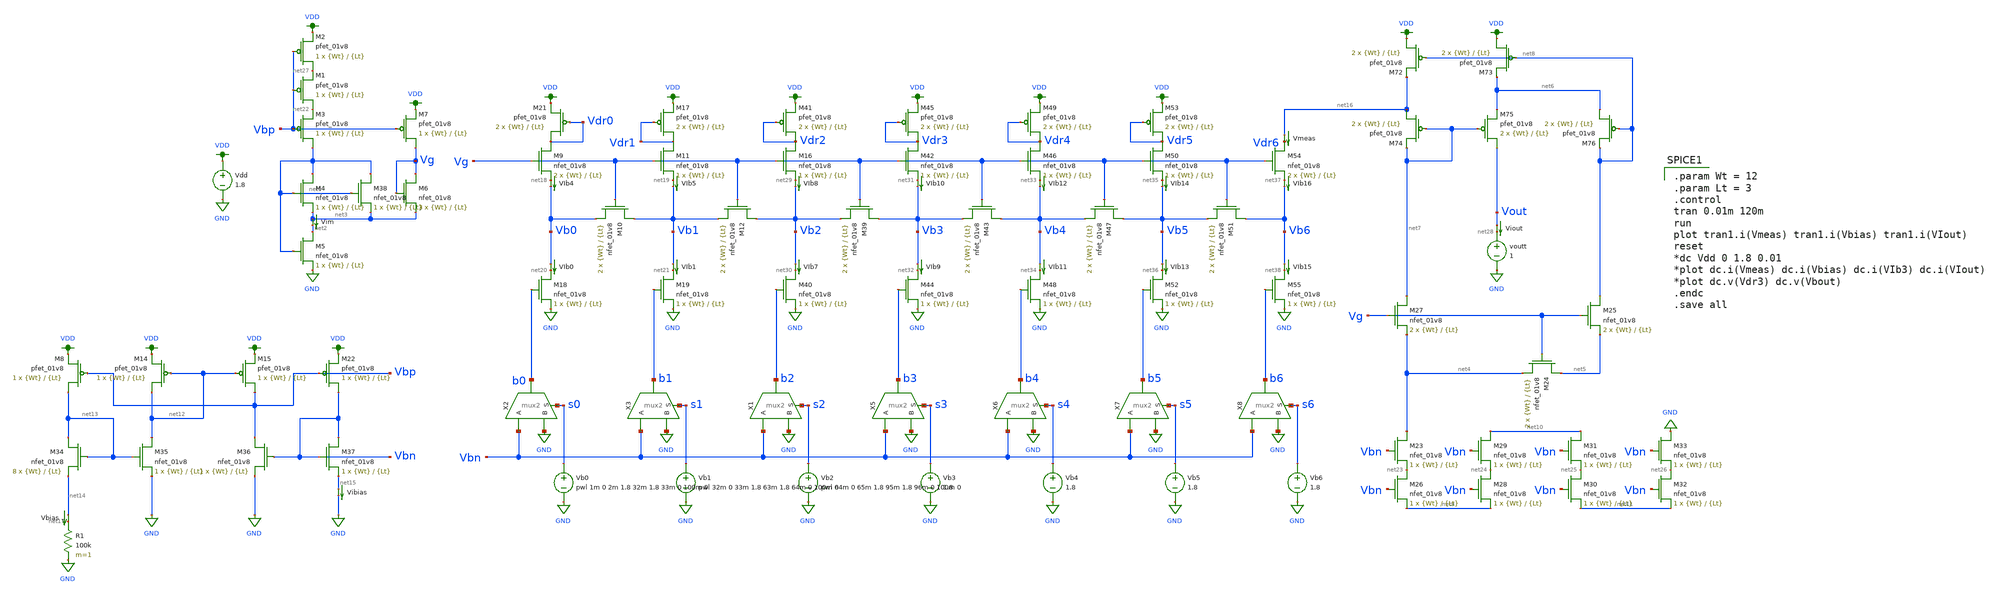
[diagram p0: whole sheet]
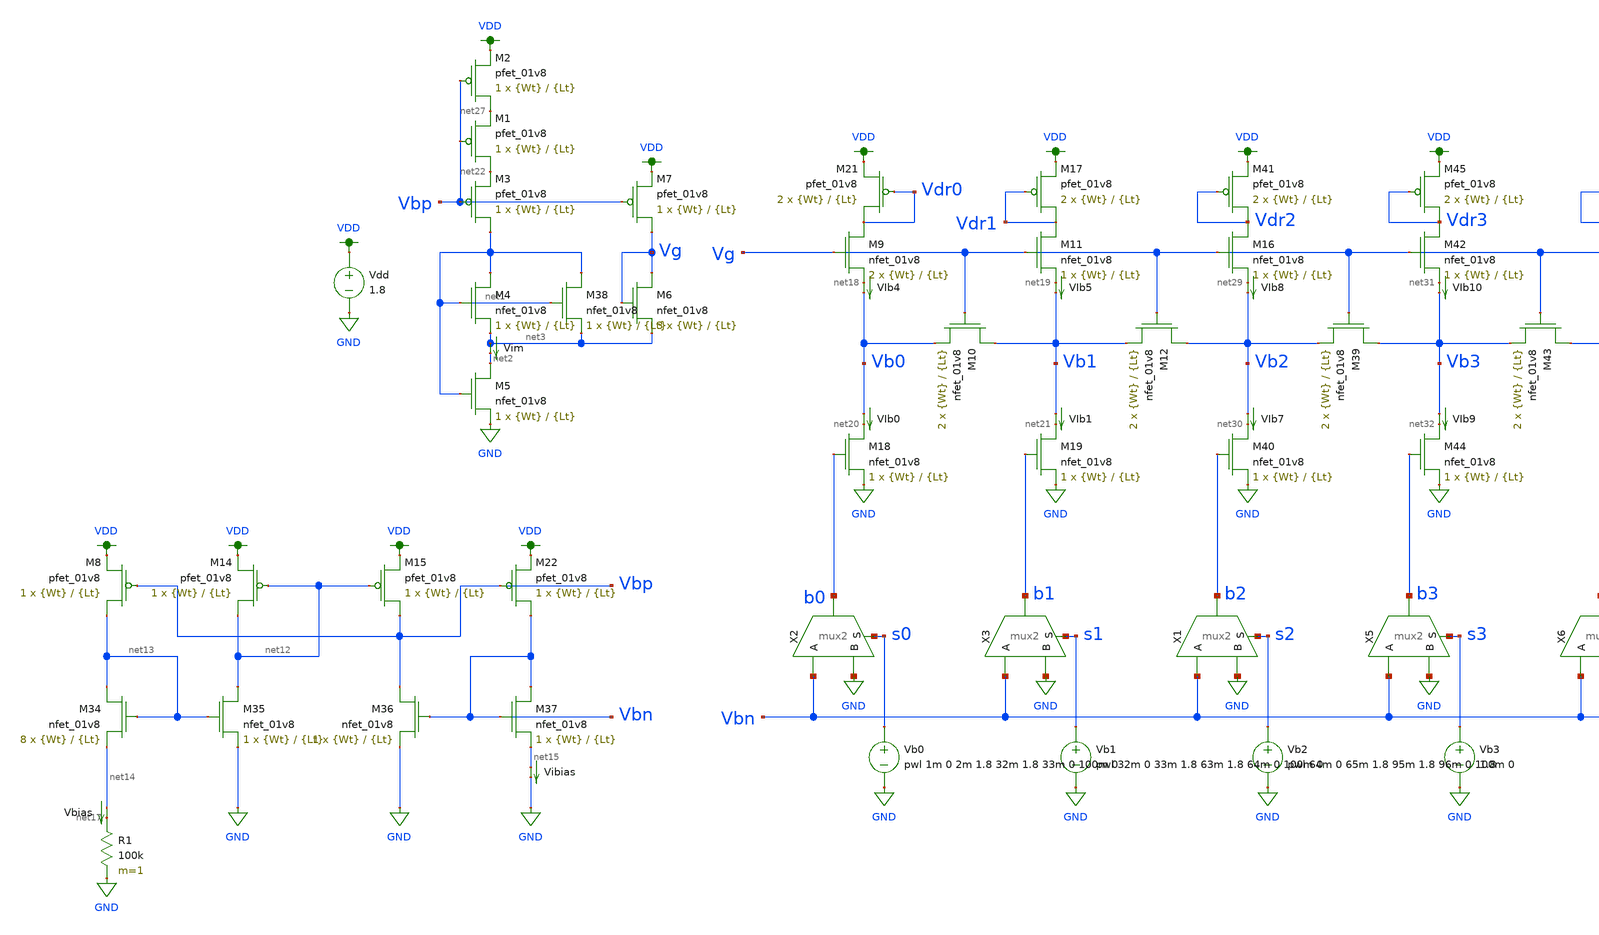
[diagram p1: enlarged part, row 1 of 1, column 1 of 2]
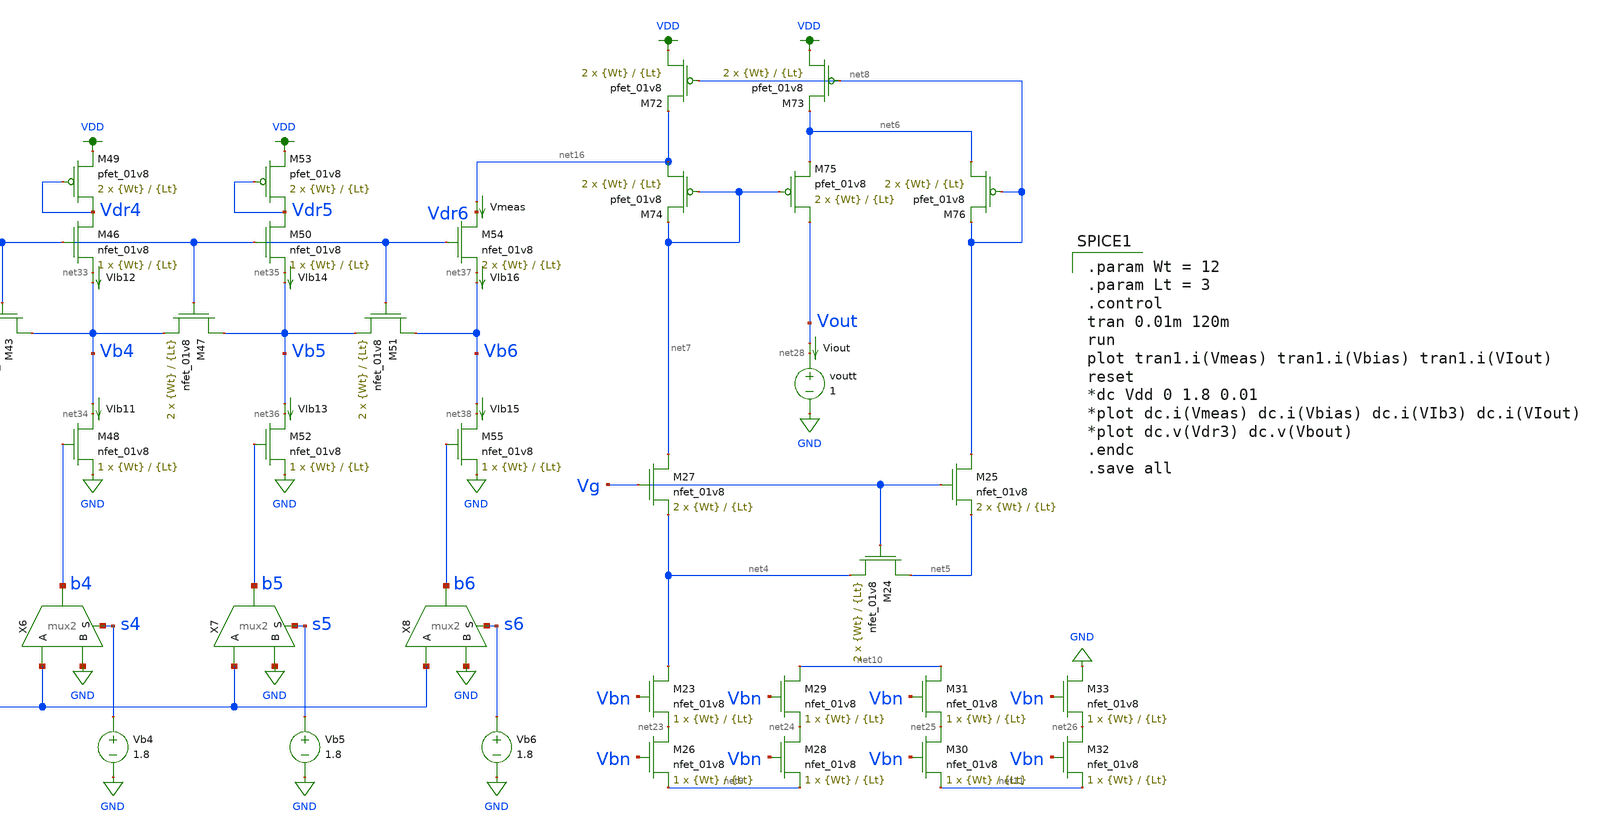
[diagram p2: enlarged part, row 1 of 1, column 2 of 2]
** sch_path: schematic/archive/dac7_test_SL_dynamic.sch
**.subckt dac7_test_SL_dynamic
X2 b0 Vbn GND s0 mux2
X3 b1 Vbn GND s1 mux2
R1 net17 GND 100k m=1
Vdd VDD GND 1.8
Vb0 s0 GND pwl 1m 0 2m 1.8 32m 1.8 33m 0 100m 0
Vb1 s1 GND pwl 32m 0 33m 1.8 63m 1.8 64m 0 100m 0
XM9 Vdr0 Vg net18 GND sky130_fd_pr__nfet_01v8 L={Lt} W={Wt} nf=1 ad='int((nf+1)/2) * W/nf * 0.29' as='int((nf+2)/2) * W/nf * 0.29'
+ pd='2*int((nf+1)/2) * (W/nf + 0.29)' ps='2*int((nf+2)/2) * (W/nf + 0.29)' nrd='0.29 / W' nrs='0.29 / W'
+ sa=0 sb=0 sd=0 mult=2 m=2
XM10 Vb1 Vg Vb0 GND sky130_fd_pr__nfet_01v8 L={Lt} W={Wt} nf=1 ad='int((nf+1)/2) * W/nf * 0.29' as='int((nf+2)/2) * W/nf * 0.29'
+ pd='2*int((nf+1)/2) * (W/nf + 0.29)' ps='2*int((nf+2)/2) * (W/nf + 0.29)' nrd='0.29 / W' nrs='0.29 / W'
+ sa=0 sb=0 sd=0 mult=2 m=2
XM11 Vdr1 Vg net19 GND sky130_fd_pr__nfet_01v8 L={Lt} W={Wt} nf=1 ad='int((nf+1)/2) * W/nf * 0.29' as='int((nf+2)/2) * W/nf * 0.29'
+ pd='2*int((nf+1)/2) * (W/nf + 0.29)' ps='2*int((nf+2)/2) * (W/nf + 0.29)' nrd='0.29 / W' nrs='0.29 / W'
+ sa=0 sb=0 sd=0 mult=1 m=1
XM12 Vb2 Vg Vb1 GND sky130_fd_pr__nfet_01v8 L={Lt} W={Wt} nf=1 ad='int((nf+1)/2) * W/nf * 0.29' as='int((nf+2)/2) * W/nf * 0.29'
+ pd='2*int((nf+1)/2) * (W/nf + 0.29)' ps='2*int((nf+2)/2) * (W/nf + 0.29)' nrd='0.29 / W' nrs='0.29 / W'
+ sa=0 sb=0 sd=0 mult=2 m=2
XM18 net20 b0 GND GND sky130_fd_pr__nfet_01v8 L={Lt} W={Wt} nf=1 ad='int((nf+1)/2) * W/nf * 0.29' as='int((nf+2)/2) * W/nf * 0.29'
+ pd='2*int((nf+1)/2) * (W/nf + 0.29)' ps='2*int((nf+2)/2) * (W/nf + 0.29)' nrd='0.29 / W' nrs='0.29 / W'
+ sa=0 sb=0 sd=0 mult=1 m=1
XM19 net21 b1 GND GND sky130_fd_pr__nfet_01v8 L={Lt} W={Wt} nf=1 ad='int((nf+1)/2) * W/nf * 0.29' as='int((nf+2)/2) * W/nf * 0.29'
+ pd='2*int((nf+1)/2) * (W/nf + 0.29)' ps='2*int((nf+2)/2) * (W/nf + 0.29)' nrd='0.29 / W' nrs='0.29 / W'
+ sa=0 sb=0 sd=0 mult=1 m=1
Vbias net14 net17 0
.save i(vbias)
VIb0 Vb0 net20 0
.save i(vib0)
VIb1 Vb1 net21 0
.save i(vib1)
XM3 net1 Vbp net22 VDD sky130_fd_pr__pfet_01v8 L={Lt} W={Wt} nf=1 ad='int((nf+1)/2) * W/nf * 0.29' as='int((nf+2)/2) * W/nf * 0.29'
+ pd='2*int((nf+1)/2) * (W/nf + 0.29)' ps='2*int((nf+2)/2) * (W/nf + 0.29)' nrd='0.29 / W' nrs='0.29 / W'
+ sa=0 sb=0 sd=0 mult=1 m=1
XM4 net1 net1 net3 GND sky130_fd_pr__nfet_01v8 L={Lt} W={Wt} nf=1 ad='int((nf+1)/2) * W/nf * 0.29' as='int((nf+2)/2) * W/nf * 0.29'
+ pd='2*int((nf+1)/2) * (W/nf + 0.29)' ps='2*int((nf+2)/2) * (W/nf + 0.29)' nrd='0.29 / W' nrs='0.29 / W'
+ sa=0 sb=0 sd=0 mult=1 m=1
XM5 net2 net1 GND GND sky130_fd_pr__nfet_01v8 L={Lt} W={Wt} nf=1 ad='int((nf+1)/2) * W/nf * 0.29' as='int((nf+2)/2) * W/nf * 0.29'
+ pd='2*int((nf+1)/2) * (W/nf + 0.29)' ps='2*int((nf+2)/2) * (W/nf + 0.29)' nrd='0.29 / W' nrs='0.29 / W'
+ sa=0 sb=0 sd=0 mult=1 m=1
Vim net3 net2 0
.save i(vim)
XM6 Vg Vg net3 GND sky130_fd_pr__nfet_01v8 L={Lt} W={Wt} nf=1 ad='int((nf+1)/2) * W/nf * 0.29' as='int((nf+2)/2) * W/nf * 0.29'
+ pd='2*int((nf+1)/2) * (W/nf + 0.29)' ps='2*int((nf+2)/2) * (W/nf + 0.29)' nrd='0.29 / W' nrs='0.29 / W'
+ sa=0 sb=0 sd=0 mult=3 m=3
XM7 Vg Vbp VDD VDD sky130_fd_pr__pfet_01v8 L={Lt} W={Wt} nf=1 ad='int((nf+1)/2) * W/nf * 0.29' as='int((nf+2)/2) * W/nf * 0.29'
+ pd='2*int((nf+1)/2) * (W/nf + 0.29)' ps='2*int((nf+2)/2) * (W/nf + 0.29)' nrd='0.29 / W' nrs='0.29 / W'
+ sa=0 sb=0 sd=0 mult=1 m=1
XM17 Vdr1 Vdr1 VDD VDD sky130_fd_pr__pfet_01v8 L={Lt} W={Wt} nf=1 ad='int((nf+1)/2) * W/nf * 0.29' as='int((nf+2)/2) * W/nf * 0.29'
+ pd='2*int((nf+1)/2) * (W/nf + 0.29)' ps='2*int((nf+2)/2) * (W/nf + 0.29)' nrd='0.29 / W' nrs='0.29 / W'
+ sa=0 sb=0 sd=0 mult=2 m=2
XM21 Vdr0 Vdr0 VDD VDD sky130_fd_pr__pfet_01v8 L={Lt} W={Wt} nf=1 ad='int((nf+1)/2) * W/nf * 0.29' as='int((nf+2)/2) * W/nf * 0.29'
+ pd='2*int((nf+1)/2) * (W/nf + 0.29)' ps='2*int((nf+2)/2) * (W/nf + 0.29)' nrd='0.29 / W' nrs='0.29 / W'
+ sa=0 sb=0 sd=0 mult=2 m=2
VIb4 net18 Vb0 0
.save i(vib4)
VIb5 net19 Vb1 0
.save i(vib5)
XM24 net5 Vg net4 GND sky130_fd_pr__nfet_01v8 L={Lt} W={Wt} nf=1 ad='int((nf+1)/2) * W/nf * 0.29' as='int((nf+2)/2) * W/nf * 0.29'
+ pd='2*int((nf+1)/2) * (W/nf + 0.29)' ps='2*int((nf+2)/2) * (W/nf + 0.29)' nrd='0.29 / W' nrs='0.29 / W'
+ sa=0 sb=0 sd=0 mult=2 m=2
XM25 net8 Vg net5 GND sky130_fd_pr__nfet_01v8 L={Lt} W={Wt} nf=1 ad='int((nf+1)/2) * W/nf * 0.29' as='int((nf+2)/2) * W/nf * 0.29'
+ pd='2*int((nf+1)/2) * (W/nf + 0.29)' ps='2*int((nf+2)/2) * (W/nf + 0.29)' nrd='0.29 / W' nrs='0.29 / W'
+ sa=0 sb=0 sd=0 mult=2 m=2
XM26 net23 Vbn net9 GND sky130_fd_pr__nfet_01v8 L={Lt} W={Wt} nf=1 ad='int((nf+1)/2) * W/nf * 0.29' as='int((nf+2)/2) * W/nf * 0.29'
+ pd='2*int((nf+1)/2) * (W/nf + 0.29)' ps='2*int((nf+2)/2) * (W/nf + 0.29)' nrd='0.29 / W' nrs='0.29 / W'
+ sa=0 sb=0 sd=0 mult=1 m=1
XM27 net7 Vg net4 GND sky130_fd_pr__nfet_01v8 L={Lt} W={Wt} nf=1 ad='int((nf+1)/2) * W/nf * 0.29' as='int((nf+2)/2) * W/nf * 0.29'
+ pd='2*int((nf+1)/2) * (W/nf + 0.29)' ps='2*int((nf+2)/2) * (W/nf + 0.29)' nrd='0.29 / W' nrs='0.29 / W'
+ sa=0 sb=0 sd=0 mult=2 m=2
XM72 VDD net8 net16 VDD sky130_fd_pr__pfet_01v8 L={Lt} W={Wt} nf=1 ad='int((nf+1)/2) * W/nf * 0.29' as='int((nf+2)/2) * W/nf * 0.29'
+ pd='2*int((nf+1)/2) * (W/nf + 0.29)' ps='2*int((nf+2)/2) * (W/nf + 0.29)' nrd='0.29 / W' nrs='0.29 / W'
+ sa=0 sb=0 sd=0 mult=2 m=2
XM73 VDD net8 net6 VDD sky130_fd_pr__pfet_01v8 L={Lt} W={Wt} nf=1 ad='int((nf+1)/2) * W/nf * 0.29' as='int((nf+2)/2) * W/nf * 0.29'
+ pd='2*int((nf+1)/2) * (W/nf + 0.29)' ps='2*int((nf+2)/2) * (W/nf + 0.29)' nrd='0.29 / W' nrs='0.29 / W'
+ sa=0 sb=0 sd=0 mult=2 m=2
XM74 net16 net7 net7 VDD sky130_fd_pr__pfet_01v8 L={Lt} W={Wt} nf=1 ad='int((nf+1)/2) * W/nf * 0.29'
+ as='int((nf+2)/2) * W/nf * 0.29' pd='2*int((nf+1)/2) * (W/nf + 0.29)' ps='2*int((nf+2)/2) * (W/nf + 0.29)'
+ nrd='0.29 / W' nrs='0.29 / W' sa=0 sb=0 sd=0 mult=2 m=2
XM75 Vout net7 net6 VDD sky130_fd_pr__pfet_01v8 L={Lt} W={Wt} nf=1 ad='int((nf+1)/2) * W/nf * 0.29' as='int((nf+2)/2) * W/nf * 0.29'
+ pd='2*int((nf+1)/2) * (W/nf + 0.29)' ps='2*int((nf+2)/2) * (W/nf + 0.29)' nrd='0.29 / W' nrs='0.29 / W'
+ sa=0 sb=0 sd=0 mult=2 m=2
XM76 net6 net8 net8 VDD sky130_fd_pr__pfet_01v8 L={Lt} W={Wt} nf=1 ad='int((nf+1)/2) * W/nf * 0.29' as='int((nf+2)/2) * W/nf * 0.29'
+ pd='2*int((nf+1)/2) * (W/nf + 0.29)' ps='2*int((nf+2)/2) * (W/nf + 0.29)' nrd='0.29 / W' nrs='0.29 / W'
+ sa=0 sb=0 sd=0 mult=2 m=2
XM23 net4 Vbn net23 GND sky130_fd_pr__nfet_01v8 L={Lt} W={Wt} nf=1 ad='int((nf+1)/2) * W/nf * 0.29' as='int((nf+2)/2) * W/nf * 0.29'
+ pd='2*int((nf+1)/2) * (W/nf + 0.29)' ps='2*int((nf+2)/2) * (W/nf + 0.29)' nrd='0.29 / W' nrs='0.29 / W'
+ sa=0 sb=0 sd=0 mult=1 m=1
XM28 net24 Vbn net9 GND sky130_fd_pr__nfet_01v8 L={Lt} W={Wt} nf=1 ad='int((nf+1)/2) * W/nf * 0.29' as='int((nf+2)/2) * W/nf * 0.29'
+ pd='2*int((nf+1)/2) * (W/nf + 0.29)' ps='2*int((nf+2)/2) * (W/nf + 0.29)' nrd='0.29 / W' nrs='0.29 / W'
+ sa=0 sb=0 sd=0 mult=1 m=1
XM29 net10 Vbn net24 GND sky130_fd_pr__nfet_01v8 L={Lt} W={Wt} nf=1 ad='int((nf+1)/2) * W/nf * 0.29'
+ as='int((nf+2)/2) * W/nf * 0.29' pd='2*int((nf+1)/2) * (W/nf + 0.29)' ps='2*int((nf+2)/2) * (W/nf + 0.29)'
+ nrd='0.29 / W' nrs='0.29 / W' sa=0 sb=0 sd=0 mult=1 m=1
XM30 net25 Vbn net11 GND sky130_fd_pr__nfet_01v8 L={Lt} W={Wt} nf=1 ad='int((nf+1)/2) * W/nf * 0.29'
+ as='int((nf+2)/2) * W/nf * 0.29' pd='2*int((nf+1)/2) * (W/nf + 0.29)' ps='2*int((nf+2)/2) * (W/nf + 0.29)'
+ nrd='0.29 / W' nrs='0.29 / W' sa=0 sb=0 sd=0 mult=1 m=1
XM31 net10 Vbn net25 GND sky130_fd_pr__nfet_01v8 L={Lt} W={Wt} nf=1 ad='int((nf+1)/2) * W/nf * 0.29'
+ as='int((nf+2)/2) * W/nf * 0.29' pd='2*int((nf+1)/2) * (W/nf + 0.29)' ps='2*int((nf+2)/2) * (W/nf + 0.29)'
+ nrd='0.29 / W' nrs='0.29 / W' sa=0 sb=0 sd=0 mult=1 m=1
XM32 net26 Vbn net11 GND sky130_fd_pr__nfet_01v8 L={Lt} W={Wt} nf=1 ad='int((nf+1)/2) * W/nf * 0.29'
+ as='int((nf+2)/2) * W/nf * 0.29' pd='2*int((nf+1)/2) * (W/nf + 0.29)' ps='2*int((nf+2)/2) * (W/nf + 0.29)'
+ nrd='0.29 / W' nrs='0.29 / W' sa=0 sb=0 sd=0 mult=1 m=1
XM33 GND Vbn net26 GND sky130_fd_pr__nfet_01v8 L={Lt} W={Wt} nf=1 ad='int((nf+1)/2) * W/nf * 0.29' as='int((nf+2)/2) * W/nf * 0.29'
+ pd='2*int((nf+1)/2) * (W/nf + 0.29)' ps='2*int((nf+2)/2) * (W/nf + 0.29)' nrd='0.29 / W' nrs='0.29 / W'
+ sa=0 sb=0 sd=0 mult=1 m=1
XM8 net13 Vbp VDD VDD sky130_fd_pr__pfet_01v8 L={Lt} W={Wt} nf=1 ad='int((nf+1)/2) * W/nf * 0.29' as='int((nf+2)/2) * W/nf * 0.29'
+ pd='2*int((nf+1)/2) * (W/nf + 0.29)' ps='2*int((nf+2)/2) * (W/nf + 0.29)' nrd='0.29 / W' nrs='0.29 / W'
+ sa=0 sb=0 sd=0 mult=1 m=1
XM14 net12 net12 VDD VDD sky130_fd_pr__pfet_01v8 L={Lt} W={Wt} nf=1 ad='int((nf+1)/2) * W/nf * 0.29'
+ as='int((nf+2)/2) * W/nf * 0.29' pd='2*int((nf+1)/2) * (W/nf + 0.29)' ps='2*int((nf+2)/2) * (W/nf + 0.29)'
+ nrd='0.29 / W' nrs='0.29 / W' sa=0 sb=0 sd=0 mult=1 m=1
XM15 Vbp net12 VDD VDD sky130_fd_pr__pfet_01v8 L={Lt} W={Wt} nf=1 ad='int((nf+1)/2) * W/nf * 0.29' as='int((nf+2)/2) * W/nf * 0.29'
+ pd='2*int((nf+1)/2) * (W/nf + 0.29)' ps='2*int((nf+2)/2) * (W/nf + 0.29)' nrd='0.29 / W' nrs='0.29 / W'
+ sa=0 sb=0 sd=0 mult=1 m=1
XM22 Vbn Vbp VDD VDD sky130_fd_pr__pfet_01v8 L={Lt} W={Wt} nf=1 ad='int((nf+1)/2) * W/nf * 0.29' as='int((nf+2)/2) * W/nf * 0.29'
+ pd='2*int((nf+1)/2) * (W/nf + 0.29)' ps='2*int((nf+2)/2) * (W/nf + 0.29)' nrd='0.29 / W' nrs='0.29 / W'
+ sa=0 sb=0 sd=0 mult=1 m=1
XM34 net13 net13 net14 GND sky130_fd_pr__nfet_01v8 L={Lt} W={Wt} nf=1 ad='int((nf+1)/2) * W/nf * 0.29'
+ as='int((nf+2)/2) * W/nf * 0.29' pd='2*int((nf+1)/2) * (W/nf + 0.29)' ps='2*int((nf+2)/2) * (W/nf + 0.29)'
+ nrd='0.29 / W' nrs='0.29 / W' sa=0 sb=0 sd=0 mult=8 m=8
XM35 net12 net13 GND GND sky130_fd_pr__nfet_01v8 L={Lt} W={Wt} nf=1 ad='int((nf+1)/2) * W/nf * 0.29'
+ as='int((nf+2)/2) * W/nf * 0.29' pd='2*int((nf+1)/2) * (W/nf + 0.29)' ps='2*int((nf+2)/2) * (W/nf + 0.29)'
+ nrd='0.29 / W' nrs='0.29 / W' sa=0 sb=0 sd=0 mult=1 m=1
XM36 Vbp Vbn GND GND sky130_fd_pr__nfet_01v8 L={Lt} W={Wt} nf=1 ad='int((nf+1)/2) * W/nf * 0.29' as='int((nf+2)/2) * W/nf * 0.29'
+ pd='2*int((nf+1)/2) * (W/nf + 0.29)' ps='2*int((nf+2)/2) * (W/nf + 0.29)' nrd='0.29 / W' nrs='0.29 / W'
+ sa=0 sb=0 sd=0 mult=1 m=1
XM37 Vbn Vbn net15 GND sky130_fd_pr__nfet_01v8 L={Lt} W={Wt} nf=1 ad='int((nf+1)/2) * W/nf * 0.29' as='int((nf+2)/2) * W/nf * 0.29'
+ pd='2*int((nf+1)/2) * (W/nf + 0.29)' ps='2*int((nf+2)/2) * (W/nf + 0.29)' nrd='0.29 / W' nrs='0.29 / W'
+ sa=0 sb=0 sd=0 mult=1 m=1
Vibias net15 GND 0
.save i(vibias)
XM1 net22 Vbp net27 VDD sky130_fd_pr__pfet_01v8 L={Lt} W={Wt} nf=1 ad='int((nf+1)/2) * W/nf * 0.29' as='int((nf+2)/2) * W/nf * 0.29'
+ pd='2*int((nf+1)/2) * (W/nf + 0.29)' ps='2*int((nf+2)/2) * (W/nf + 0.29)' nrd='0.29 / W' nrs='0.29 / W'
+ sa=0 sb=0 sd=0 mult=1 m=1
XM2 net27 Vbp VDD VDD sky130_fd_pr__pfet_01v8 L={Lt} W={Wt} nf=1 ad='int((nf+1)/2) * W/nf * 0.29' as='int((nf+2)/2) * W/nf * 0.29'
+ pd='2*int((nf+1)/2) * (W/nf + 0.29)' ps='2*int((nf+2)/2) * (W/nf + 0.29)' nrd='0.29 / W' nrs='0.29 / W'
+ sa=0 sb=0 sd=0 mult=1 m=1
XM38 net1 net1 net3 GND sky130_fd_pr__nfet_01v8 L={Lt} W={Wt} nf=1 ad='int((nf+1)/2) * W/nf * 0.29' as='int((nf+2)/2) * W/nf * 0.29'
+ pd='2*int((nf+1)/2) * (W/nf + 0.29)' ps='2*int((nf+2)/2) * (W/nf + 0.29)' nrd='0.29 / W' nrs='0.29 / W'
+ sa=0 sb=0 sd=0 mult=1 m=1
voutt net28 GND 1
X1 b2 Vbn GND s2 mux2
Vb3 s3 GND 1.8
XM16 Vdr2 Vg net29 GND sky130_fd_pr__nfet_01v8 L={Lt} W={Wt} nf=1 ad='int((nf+1)/2) * W/nf * 0.29' as='int((nf+2)/2) * W/nf * 0.29'
+ pd='2*int((nf+1)/2) * (W/nf + 0.29)' ps='2*int((nf+2)/2) * (W/nf + 0.29)' nrd='0.29 / W' nrs='0.29 / W'
+ sa=0 sb=0 sd=0 mult=1 m=1
XM39 Vb3 Vg Vb2 GND sky130_fd_pr__nfet_01v8 L={Lt} W={Wt} nf=1 ad='int((nf+1)/2) * W/nf * 0.29' as='int((nf+2)/2) * W/nf * 0.29'
+ pd='2*int((nf+1)/2) * (W/nf + 0.29)' ps='2*int((nf+2)/2) * (W/nf + 0.29)' nrd='0.29 / W' nrs='0.29 / W'
+ sa=0 sb=0 sd=0 mult=2 m=2
XM40 net30 b2 GND GND sky130_fd_pr__nfet_01v8 L={Lt} W={Wt} nf=1 ad='int((nf+1)/2) * W/nf * 0.29' as='int((nf+2)/2) * W/nf * 0.29'
+ pd='2*int((nf+1)/2) * (W/nf + 0.29)' ps='2*int((nf+2)/2) * (W/nf + 0.29)' nrd='0.29 / W' nrs='0.29 / W'
+ sa=0 sb=0 sd=0 mult=1 m=1
VIb7 Vb2 net30 0
.save i(vib7)
XM41 Vdr2 Vdr2 VDD VDD sky130_fd_pr__pfet_01v8 L={Lt} W={Wt} nf=1 ad='int((nf+1)/2) * W/nf * 0.29' as='int((nf+2)/2) * W/nf * 0.29'
+ pd='2*int((nf+1)/2) * (W/nf + 0.29)' ps='2*int((nf+2)/2) * (W/nf + 0.29)' nrd='0.29 / W' nrs='0.29 / W'
+ sa=0 sb=0 sd=0 mult=2 m=2
VIb8 net29 Vb2 0
.save i(vib8)
X5 b3 Vbn GND s3 mux2
Vb4 s4 GND 1.8
XM42 Vdr3 Vg net31 GND sky130_fd_pr__nfet_01v8 L={Lt} W={Wt} nf=1 ad='int((nf+1)/2) * W/nf * 0.29' as='int((nf+2)/2) * W/nf * 0.29'
+ pd='2*int((nf+1)/2) * (W/nf + 0.29)' ps='2*int((nf+2)/2) * (W/nf + 0.29)' nrd='0.29 / W' nrs='0.29 / W'
+ sa=0 sb=0 sd=0 mult=1 m=1
XM43 Vb4 Vg Vb3 GND sky130_fd_pr__nfet_01v8 L={Lt} W={Wt} nf=1 ad='int((nf+1)/2) * W/nf * 0.29' as='int((nf+2)/2) * W/nf * 0.29'
+ pd='2*int((nf+1)/2) * (W/nf + 0.29)' ps='2*int((nf+2)/2) * (W/nf + 0.29)' nrd='0.29 / W' nrs='0.29 / W'
+ sa=0 sb=0 sd=0 mult=2 m=2
XM44 net32 b3 GND GND sky130_fd_pr__nfet_01v8 L={Lt} W={Wt} nf=1 ad='int((nf+1)/2) * W/nf * 0.29' as='int((nf+2)/2) * W/nf * 0.29'
+ pd='2*int((nf+1)/2) * (W/nf + 0.29)' ps='2*int((nf+2)/2) * (W/nf + 0.29)' nrd='0.29 / W' nrs='0.29 / W'
+ sa=0 sb=0 sd=0 mult=1 m=1
VIb9 Vb3 net32 0
.save i(vib9)
XM45 Vdr3 Vdr3 VDD VDD sky130_fd_pr__pfet_01v8 L={Lt} W={Wt} nf=1 ad='int((nf+1)/2) * W/nf * 0.29' as='int((nf+2)/2) * W/nf * 0.29'
+ pd='2*int((nf+1)/2) * (W/nf + 0.29)' ps='2*int((nf+2)/2) * (W/nf + 0.29)' nrd='0.29 / W' nrs='0.29 / W'
+ sa=0 sb=0 sd=0 mult=2 m=2
VIb10 net31 Vb3 0
.save i(vib10)
X6 b4 Vbn GND s4 mux2
Vb5 s5 GND 1.8
XM46 Vdr4 Vg net33 GND sky130_fd_pr__nfet_01v8 L={Lt} W={Wt} nf=1 ad='int((nf+1)/2) * W/nf * 0.29' as='int((nf+2)/2) * W/nf * 0.29'
+ pd='2*int((nf+1)/2) * (W/nf + 0.29)' ps='2*int((nf+2)/2) * (W/nf + 0.29)' nrd='0.29 / W' nrs='0.29 / W'
+ sa=0 sb=0 sd=0 mult=1 m=1
XM47 Vb5 Vg Vb4 GND sky130_fd_pr__nfet_01v8 L={Lt} W={Wt} nf=1 ad='int((nf+1)/2) * W/nf * 0.29' as='int((nf+2)/2) * W/nf * 0.29'
+ pd='2*int((nf+1)/2) * (W/nf + 0.29)' ps='2*int((nf+2)/2) * (W/nf + 0.29)' nrd='0.29 / W' nrs='0.29 / W'
+ sa=0 sb=0 sd=0 mult=2 m=2
XM48 net34 b4 GND GND sky130_fd_pr__nfet_01v8 L={Lt} W={Wt} nf=1 ad='int((nf+1)/2) * W/nf * 0.29' as='int((nf+2)/2) * W/nf * 0.29'
+ pd='2*int((nf+1)/2) * (W/nf + 0.29)' ps='2*int((nf+2)/2) * (W/nf + 0.29)' nrd='0.29 / W' nrs='0.29 / W'
+ sa=0 sb=0 sd=0 mult=1 m=1
VIb11 Vb4 net34 0
.save i(vib11)
XM49 Vdr4 Vdr4 VDD VDD sky130_fd_pr__pfet_01v8 L={Lt} W={Wt} nf=1 ad='int((nf+1)/2) * W/nf * 0.29' as='int((nf+2)/2) * W/nf * 0.29'
+ pd='2*int((nf+1)/2) * (W/nf + 0.29)' ps='2*int((nf+2)/2) * (W/nf + 0.29)' nrd='0.29 / W' nrs='0.29 / W'
+ sa=0 sb=0 sd=0 mult=2 m=2
VIb12 net33 Vb4 0
.save i(vib12)
X7 b5 Vbn GND s5 mux2
Vb6 s6 GND 1.8
XM50 Vdr5 Vg net35 GND sky130_fd_pr__nfet_01v8 L={Lt} W={Wt} nf=1 ad='int((nf+1)/2) * W/nf * 0.29' as='int((nf+2)/2) * W/nf * 0.29'
+ pd='2*int((nf+1)/2) * (W/nf + 0.29)' ps='2*int((nf+2)/2) * (W/nf + 0.29)' nrd='0.29 / W' nrs='0.29 / W'
+ sa=0 sb=0 sd=0 mult=1 m=1
XM51 Vb6 Vg Vb5 GND sky130_fd_pr__nfet_01v8 L={Lt} W={Wt} nf=1 ad='int((nf+1)/2) * W/nf * 0.29' as='int((nf+2)/2) * W/nf * 0.29'
+ pd='2*int((nf+1)/2) * (W/nf + 0.29)' ps='2*int((nf+2)/2) * (W/nf + 0.29)' nrd='0.29 / W' nrs='0.29 / W'
+ sa=0 sb=0 sd=0 mult=2 m=2
XM52 net36 b5 GND GND sky130_fd_pr__nfet_01v8 L={Lt} W={Wt} nf=1 ad='int((nf+1)/2) * W/nf * 0.29' as='int((nf+2)/2) * W/nf * 0.29'
+ pd='2*int((nf+1)/2) * (W/nf + 0.29)' ps='2*int((nf+2)/2) * (W/nf + 0.29)' nrd='0.29 / W' nrs='0.29 / W'
+ sa=0 sb=0 sd=0 mult=1 m=1
VIb13 Vb5 net36 0
.save i(vib13)
XM53 Vdr5 Vdr5 VDD VDD sky130_fd_pr__pfet_01v8 L={Lt} W={Wt} nf=1 ad='int((nf+1)/2) * W/nf * 0.29' as='int((nf+2)/2) * W/nf * 0.29'
+ pd='2*int((nf+1)/2) * (W/nf + 0.29)' ps='2*int((nf+2)/2) * (W/nf + 0.29)' nrd='0.29 / W' nrs='0.29 / W'
+ sa=0 sb=0 sd=0 mult=2 m=2
VIb14 net35 Vb5 0
.save i(vib14)
X8 b6 Vbn GND s6 mux2
XM54 Vdr6 Vg net37 GND sky130_fd_pr__nfet_01v8 L={Lt} W={Wt} nf=1 ad='int((nf+1)/2) * W/nf * 0.29' as='int((nf+2)/2) * W/nf * 0.29'
+ pd='2*int((nf+1)/2) * (W/nf + 0.29)' ps='2*int((nf+2)/2) * (W/nf + 0.29)' nrd='0.29 / W' nrs='0.29 / W'
+ sa=0 sb=0 sd=0 mult=2 m=2
XM55 net38 b6 GND GND sky130_fd_pr__nfet_01v8 L={Lt} W={Wt} nf=1 ad='int((nf+1)/2) * W/nf * 0.29' as='int((nf+2)/2) * W/nf * 0.29'
+ pd='2*int((nf+1)/2) * (W/nf + 0.29)' ps='2*int((nf+2)/2) * (W/nf + 0.29)' nrd='0.29 / W' nrs='0.29 / W'
+ sa=0 sb=0 sd=0 mult=1 m=1
Vmeas net16 Vdr6 0
.save i(vmeas)
VIb15 Vb6 net38 0
.save i(vib15)
VIb16 net37 Vb6 0
.save i(vib16)
Vb2 s2 GND pwl 64m 0 65m 1.8 95m 1.8 96m 0 100m 0
Viout Vout net28 0
.save i(viout)
**** begin user architecture code

.option wnflag=1
.param MC_SWITCH=1.0
.lib ~/skywater/skywater-pdk/libraries/sky130_fd_pr_ngspice/latest/models/sky130.lib.spice tt


.param Wt = 12
.param Lt = 3
.control
tran 0.01m 120m
run
plot tran1.i(Vmeas) tran1.i(Vbias) tran1.i(VIout)
reset
*dc Vdd 0 1.8 0.01
*plot dc.i(Vmeas) dc.i(Vbias) dc.i(VIb3) dc.i(VIout)
*plot dc.v(Vdr3) dc.v(Vbout)
.endc
.save all

**** end user architecture code
**.ends
.GLOBAL GND
.GLOBAL VDD
.end
